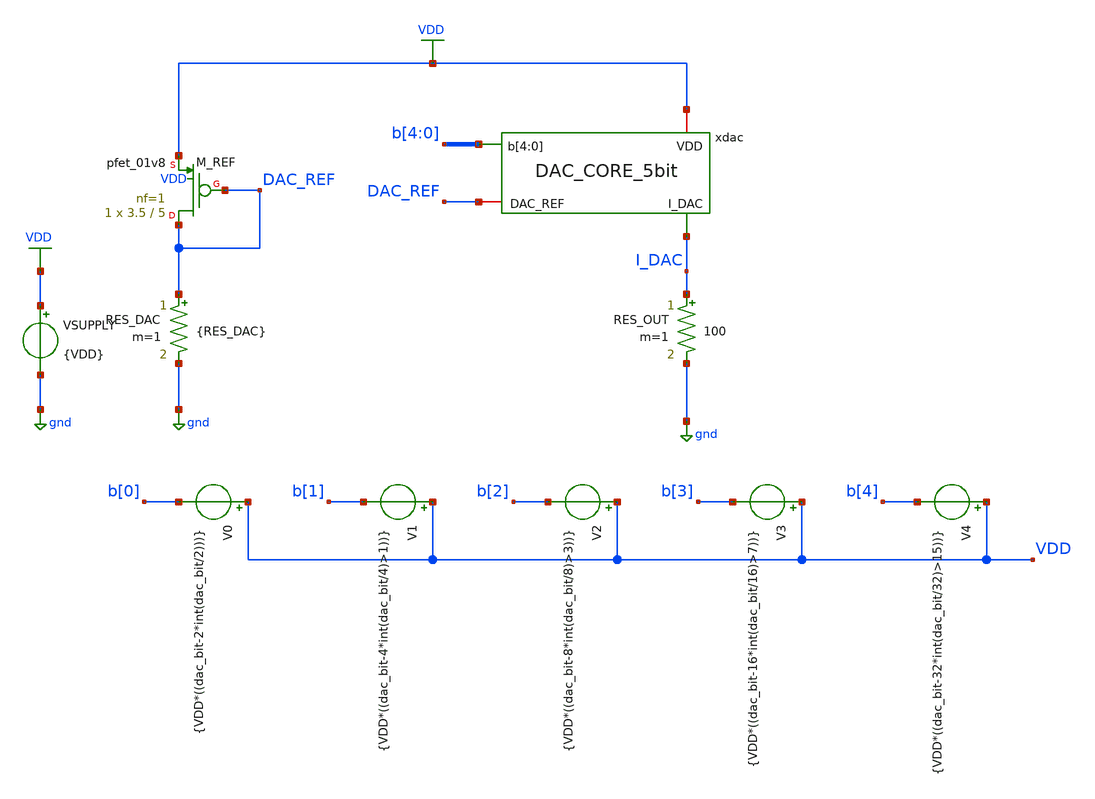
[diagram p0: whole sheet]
** sch_path: designs_backup/designs/lab2/xschem/DAC_CORE_5bit_cpyof_test.sch
**.subckt DAC_CORE_5bit_cpyof_test
RES_DAC DAC_REF gnd {RES_DAC} m=1
RES_OUT I_DAC gnd 100 m=1
V0 VDD b[0] {VDD*((dac_bit-2*int(dac_bit/2)))}
VSUPPLY VDD gnd {VDD}
V1 VDD b[1] {VDD*((dac_bit-4*int(dac_bit/4)>1))}
V2 VDD b[2] {VDD*((dac_bit-8*int(dac_bit/8)>3))}
V3 VDD b[3] {VDD*((dac_bit-16*int(dac_bit/16)>7))}
V4 VDD b[4] {VDD*((dac_bit-32*int(dac_bit/32)>15))}
XM_REF DAC_REF DAC_REF VDD VDD sky130_fd_pr__pfet_01v8 L=5 W=3.5 nf=1 ad='int((1 + 1)/2) * 3.5 / 1 * 0.29'
+ as='int((1 + 2)/2) * 3.5 / 1 * 0.29' pd='2*int((1 + 1)/2) * (3.5 / 1 + 0.29)' ps='2*int((1 + 2)/2) * (3.5 / 1 + 0.29)'
+ nrd='0.29 / 3.5 ' nrs='0.29 / 3.5 ' sa=0 sb=0 sd=0 mult=1 m=1
xdac VDD DAC_REF I_DAC b[4] b[3] b[2] b[1] b[0] DAC_CORE_5bit
**** begin user architecture code

** opencircuitdesign pdks install
.lib $::SKYWATER_MODELS/sky130.lib.spice tt

* force include MC files
.include "$::SKYWATER_MODELS/parameters/montecarlo.spice"
.include "$::SKYWATER_MODELS/parameters/critical.spice"

* force mismatch/process params
.param mc_mm_switch = 0
.param mc_pr_switch = 0

* disable pfet_ideal from mismatch/process
.subckt sky130_fd_pr__pfet_ideal D G S B W=0.42 L=0.18  nf=1 ad='int((1 + 1)/2) * {W} / 1 * 0.29' as='int((1 + 2)/2) * {W} / 1 * 0.29'
+  pd='2*int((1 + 1)/2) * ({W} / 1 + 0.29)' ps='2*int((1 + 2)/2) * ({W} / 1 + 0.29)'   nrd='0.29 / {W}'
+ nrs='0.29 / {W}' sa=0 sb=0 sd=0 mult=1
  .param mc_mm_switch=0
  .param mc_pr_switch=0
  XIDEAL D G S B sky130_fd_pr__pfet_01v8 W={W} L={L}
  + nf={nf} ad={ad} as={as} pd={pd} ps={ps}
  + nrd={nrd} nrs={nrs} sa={sa} sb={sb} sd={sd} mult={mult}
.ends



.param VDD = 1.8
.param RES_DAC = 11.37k
.param dac_bit = 0
.options savecurrents

.control
  shell mkdir -p /foss/designs/lab2/results/2.4
  shell rm -f /foss/designs/lab2/results/2.4/Idac_results_2.dat

  let d_val = 0
  reset
  op
  let Id_ref = @m.xm_ref.msky130_fd_pr__pfet_01v8[id] * 1e6
  let vth_ref = @m.xm_ref.msky130_fd_pr__pfet_01v8[vth]
  let vgs_ref = @m.xm_ref.msky130_fd_pr__pfet_01v8[vgs]
  echo -- Id_M_REF[uA]= $&Id_ref  | Vth_M_REF[V]= $&vth_ref | Vgs_M_REF[V]= $&vgs_ref -- >>
+ /foss/designs/lab2/results/2.4/Idac_results_2.dat
  echo >> /foss/designs/lab2/results/2.4/Idac_results_2.dat
  dowhile d_val <= 31
    alterparam dac_bit = $&d_val
    reset
    op
    let I_dac = @res_out[i] * 1e6
    echo dac_bit= $&d_val  |  I_dac[uA]= $&I_dac >>
+ /foss/designs/lab2/results/2.4/Idac_results_2.dat
    let d_val = $&d_val + 1
  end
.endc


**** end user architecture code
**.ends
.GLOBAL gnd
.GLOBAL VDD
.end
